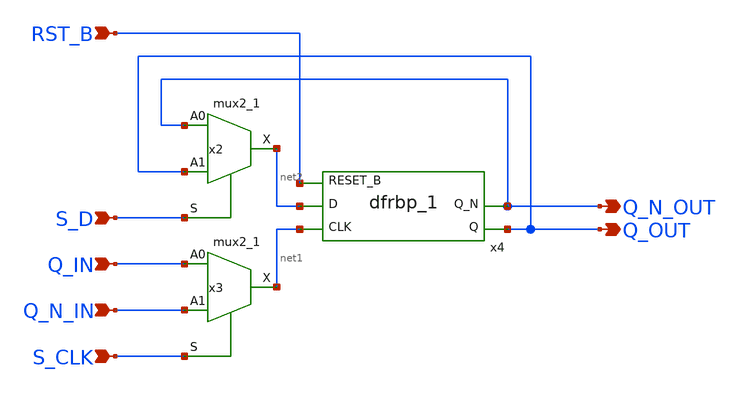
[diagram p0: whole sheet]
** sch_path: add_sub_bit.sch
**.subckt add_sub_bit S_D S_CLK Q_OUT Q_N_OUT RST_B Q_N_IN Q_IN
*.ipin S_D
*.ipin S_CLK
*.opin Q_OUT
*.opin Q_N_OUT
*.ipin RST_B
*.ipin Q_N_IN
*.ipin Q_IN
x2 Q_N_OUT Q_OUT S_D VGND VNB VPB VPWR net2 sky130_fd_sc_hd__mux2_1
x3 Q_IN Q_N_IN S_CLK VGND VNB VPB VPWR net1 sky130_fd_sc_hd__mux2_1
x4 net1 net2 RST_B VGND VNB VPB VPWR Q_OUT Q_N_OUT sky130_fd_sc_hd__dfrbp_1
**.ends
.end
